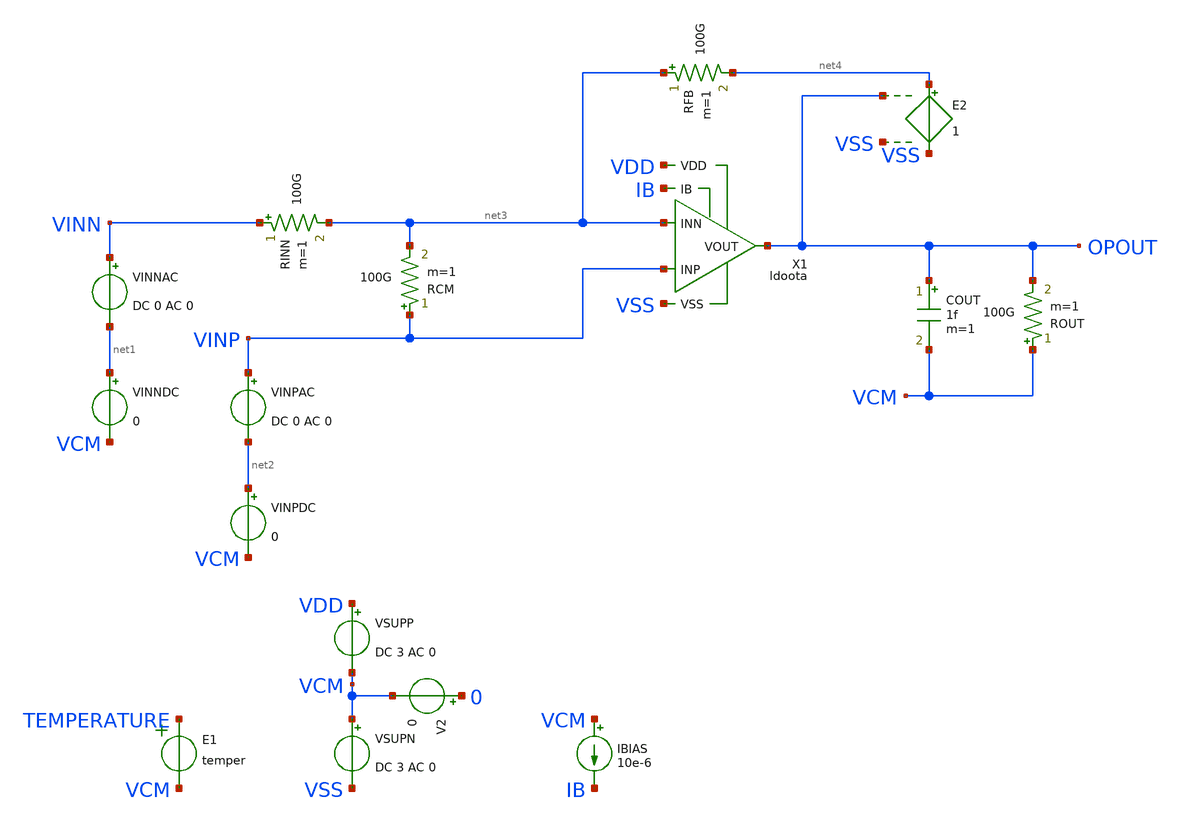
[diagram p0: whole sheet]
** sch_path: tt08/ip/ldo/xschem/ldoota_tb.sch
**.subckt ldoota_tb
V2 0 VCM 0
E1 TEMPERATURE VCM VOL=' temper '
IBIAS VCM IB 10e-6
COUT OPOUT VCM 1f m=1
VINNDC net1 VCM 0
VINNAC VINN net1 DC 0 AC 0
VINPDC net2 VCM 0
VINPAC VINP net2 DC 0 AC 0
ROUT VCM OPOUT 100G m=1
VSUPP VDD VCM DC 3 AC 0
RFB net3 net4 100G m=1
RINN VINN net3 100G m=1
RCM VINP net3 100G m=1
VSUPN VCM VSS DC 3 AC 0
X1 VDD VSS OPOUT IB net3 VINP ldoota
E2 net4 VSS OPOUT VSS 1
**** begin user architecture code

.csparam TB_ID=$::TB_ID\
.csparam MC_RUNS=$::MC_RUNS\
.csparam EXIT_NGSPICE=$::EXIT_NGSPICE\
.lib $::SKYWATER_MODELS/sky130.lib.spice $::CORNER\


* this experimental option enables mos model bin
* selection based on W/NF instead of W
.option wnflag=0

.control
* option savecurrents

* dummy block for goto
if (1)
if TB_ID = 0
	goto AC_INOISE
end
if TB_ID = 1
	goto AC_OL
end
if TB_ID = 2
	goto AC_CMRR_PSRR
end
if TB_ID = 3
	goto TRAN_OUTRNG
end
if TB_ID = 4
	goto TRAN_CMINP
end
if TB_ID = 5
	goto TRAN_SLEW
end
if TB_ID = 6
	goto AC_INOISE
end
if TB_ID = 7
	goto TRAN_THD
end

* Helper Functions
******************
define aunif(nom, avar) (nom+avar*sunif(0))
define agauss(nom, avar, sig) (nom + avar / sig * sgauss (0))

****************************************
label AC_OL
save all
****************************************
if MC_RUNS = 0
	let olgain_1hz = vector(MC_RUNS+1)
	let pm = vector(MC_RUNS+1)
	let ugbw = vector(MC_RUNS+1)
	let f1_3db = vector(MC_RUNS+1)
	let f2_3db = vector(MC_RUNS+1)
	let run=0

	.include ldoota_ac_ol_ops.inc

	set nobreak
	set width=300
	print col olgain_1hz, pm, ugbw, f1_3db, f2_3db > ldoota_ac_ol.csv
else
	let olgain_1hz = vector(MC_RUNS)
	let pm = vector(MC_RUNS)
	let ugbw = vector(MC_RUNS)
	let f1_3db = vector(MC_RUNS)
	let f2_3db = vector(MC_RUNS)
	let run=0
	dowhile run < MC_RUNS
		echo MC-RUN: $&run

		.include ldoota_ac_ol_ops.inc

 		reset
		let run = run + 1
	end
	set nobreak
	set width=300
	print olgain_1hz, pm, ugbw, f1_3db, f2_3db > ldoota_ac_ol.csv
end
goto done

****************************************
label AC_CMRR_PSRR
save all
****************************************
if MC_RUNS = 0
	let cmrr_10Hz = vector(MC_RUNS+1)
	let cmrr_10MHz = vector(MC_RUNS+1)
	let psrr_p_10Hz = vector(MC_RUNS+1)
	let psrr_p_10MHz = vector(MC_RUNS+1)
	let psrr_n_10Hz = vector(MC_RUNS+1)
	let psrr_n_10MHz = vector(MC_RUNS+1)
	let run=0

	.include ldoota_ac_cmrr_psrr_ops.inc

	set nobreak
	set width=300
	print col cmrr_10Hz, cmrr_10MHz, psrr_p_10Hz, psrr_p_10MHz, psrr_n_10Hz, psrr_n_10MHz >
+ ldoota_ac_cmrr_psrr.csv
else
	let cmrr_10Hz = vector(MC_RUNS)
	let cmrr_10MHz = vector(MC_RUNS)
	let psrr_p_10Hz = vector(MC_RUNS)
	let psrr_p_10MHz = vector(MC_RUNS)
	let psrr_n_10Hz = vector(MC_RUNS)
	let psrr_n_10MHz = vector(MC_RUNS)
	let run=0
	dowhile run < MC_RUNS
		echo MC-RUN: $&run

		.include ldoota_ac_cmrr_psrr_ops.inc

 		reset
		let run = run + 1
	end
	set nobreak
	set width=300
	print cmrr_10Hz, cmrr_10MHz, psrr_p_10Hz, psrr_p_10MHz, psrr_n_10Hz, psrr_n_10MHz >
+ ldoota_ac_cmrr_psrr.csv
end
goto done

****************************************
label TRAN_OUTRNG
save all
****************************************
if MC_RUNS = 0
	let neg_out_comp = vector(MC_RUNS+1)
	let pos_out_comp = vector(MC_RUNS+1)
	let run=0

	.include ldoota_tran_outrng_ops.inc

	set nobreak
	set width=300
	print col neg_out_comp, pos_out_comp > ldoota_tran_outrng.csv
else
	let neg_out_comp = vector(MC_RUNS)
	let pos_out_comp = vector(MC_RUNS)
	let run=0
	dowhile run < MC_RUNS
		echo MC-RUN: $&run

		.include ldoota_tran_outrng_ops.inc

 		reset
		let run = run + 1
	end
	set nobreak
	set width=300
	print neg_out_comp, pos_out_comp > ldoota_tran_outrng.csv
end
goto done

****************************************
label TRAN_CMINP
save all
****************************************
if MC_RUNS = 0
	let pos_cm_bound = vector(MC_RUNS+1)
	let neg_cm_bound = vector(MC_RUNS+1)
	let run=0

	.include ldoota_tran_cminp_ops.inc

	set nobreak
	set width=300
	print col pos_cm_bound, neg_cm_bound > ldoota_tran_inprng.csv
else
	let pos_cm_bound = vector(MC_RUNS)
	let neg_cm_bound = vector(MC_RUNS)
	let run=0
	dowhile run < MC_RUNS
		echo MC-RUN: $&run

		.include ldoota_tran_cminp_ops.inc

 		reset
		let run = run + 1
	end
	set nobreak
	set width=300
	print pos_cm_bound, neg_cm_bound > ldoota_tran_inprng.csv
end
goto done

****************************************
label TRAN_SLEW
save all
****************************************
if MC_RUNS = 0
	let inp_offset = vector(MC_RUNS+1)
	let slew_pos = vector(MC_RUNS+1)
	let slew_neg = vector(MC_RUNS+1)
	let run=0

	.include ldoota_tran_slew_ops.inc

	set nobreak
	set width=300
	print col inp_offset, slew_pos, slew_neg > ldoota_tran_slew.csv
else
	let inp_offset = vector(MC_RUNS)
	let slew_pos = vector(MC_RUNS)
	let slew_neg = vector(MC_RUNS)
	let run=0
	dowhile run < MC_RUNS
		echo MC-RUN: $&run

		.include ldoota_tran_slew_ops.inc

 		reset
		let run = run + 1
	end
	set nobreak
	set width=300
	print inp_offset, slew_pos, slew_neg > ldoota_tran_slew.csv
end
goto done

****************************************
label AC_INOISE
****************************************
alter vsupp dc = 3
alter vsupp ac = 0
alter vsupn dc = 3
alter vsupn ac = 0
alter vinnac ac = 0
alter vinndc dc = 0
alter vinpac ac = 0
alter vinpdc dc = 0
alter rinn resistance = 100e12
alter rinn ac = 100e12
alter rcm resistance = 100e12
alter rcm ac = 100e12
alter rfb resistance = 0.01
alter rfb ac = 0.01

noise V(OPOUT) VINPAC dec 10 1 100e6 1
print noise2.onoise_total noise2.inoise_total
if EXIT_NGSPICE = 0
	plot noise1.onoise_spectrum
	plot noise1.inoise_spectrum
end
setplot noise1
write ldoota_noise1_opout.raw all

* https://sourceforge.net/p/ngspice/discussion/120973/thread/2aa3e30f/ -- Holger Vogt
* script to read a specific y-value if x given
**********************************************
let f0 = vector(1)
let f1 = vector(1)
let n_f0 = vector(1)
let n_f1 = vector(1)
compose freq_list values 10 10e3
foreach freq_idx 0 1
	let freq = freq_list[$freq_idx]
	* find index where freqency is just above interesting value
	setplot noise1
	let nn = 0
	while frequency[nn] < freq
		let nn = nn + 1
	end
	* define vectors of frequncies and values just above and below
	* selected frequeny
	let fnn = frequency[nn]
	let nn1 = nn - 1
	let fnn1 = frequency[nn1]
	let snn = onoise_spectrum[nn]
	let snn1 = onoise_spectrum[nn1]
	*print vector values
	echo nn = $&nn  fnn = $&fnn  snn = $&snn
	echo nn1 = $&nn1  fnn1 = $&fnn1  snn1 = $&snn1
	*linear interpolation for exact frequency
	let newsnn = snn1 + (snn - snn1)/(fnn - fnn1)*(freq - fnn1)
	echo newfnn = $&freq  newsnn = $&newsnn
	if $freq_idx = 0
		let f0 = freq
		let n_f0 = newsnn
	end
	if $freq_idx = 1
		let f1 = freq
		let n_f1 = newsnn
	end
end
set nobreak
set width=300
set noprintscale
print col f0, n_f0, f1, n_f1 > ldoota_ac_inoise.csv

goto done

****************************************
label TRAN_THD
save all
****************************************
if MC_RUNS = 0
	let thd = vector(MC_RUNS+1)
	let run=0

	.include ldoota_tran_thd_ops.inc

	set nobreak
	set width=300
	print col thd > ldoota_tran_thd.csv
else
	let thd = vector(MC_RUNS)
	let run=0
	dowhile run < MC_RUNS
		echo MC-RUN: $&run

		reset

		.include ldoota_tran_thd_ops.inc

		let run = run + 1
	end
	set nobreak
	set width=300
	print thd > ldoota_tran_thd.csv
end
goto done

****************************************
label done
****************************************
if EXIT_NGSPICE > 0.0
	exit
end
end
.endc


**** end user architecture code
**.ends

* expanding   symbol:  ldoota.sym # of pins=6
** sym_path: ldoota.sym
** sch_path: ldoota.sch
.subckt ldoota VDD VSS VOUT IB INN INP
*.ipin IB
*.iopin VDD
*.iopin VSS
*.iopin INP
*.iopin INN
*.iopin VOUT
XMMIRL net1 net1 VDD VDD sky130_fd_pr__pfet_g5v0d10v5 L=2 W=20 nf=1 ad='int((nf+1)/2) * W/nf * 0.29'
+ as='int((nf+2)/2) * W/nf * 0.29' pd='2*int((nf+1)/2) * (W/nf + 0.29)' ps='2*int((nf+2)/2) * (W/nf + 0.29)'
+ nrd='0.29 / W' nrs='0.29 / W' sa=0 sb=0 sd=0 mult=1 m=1
XMMIRR net2 net2 VDD VDD sky130_fd_pr__pfet_g5v0d10v5 L=2 W=20 nf=1 ad='int((nf+1)/2) * W/nf * 0.29'
+ as='int((nf+2)/2) * W/nf * 0.29' pd='2*int((nf+1)/2) * (W/nf + 0.29)' ps='2*int((nf+2)/2) * (W/nf + 0.29)'
+ nrd='0.29 / W' nrs='0.29 / W' sa=0 sb=0 sd=0 mult=1 m=1
XMDR net2 INN net3 VSS sky130_fd_pr__nfet_g5v0d10v5 L=2 W=20 nf=1 ad='int((nf+1)/2) * W/nf * 0.29' as='int((nf+2)/2) * W/nf * 0.29'
+ pd='2*int((nf+1)/2) * (W/nf + 0.29)' ps='2*int((nf+2)/2) * (W/nf + 0.29)' nrd='0.29 / W' nrs='0.29 / W'
+ sa=0 sb=0 sd=0 mult=5 m=5
XMDL net1 INP net3 VSS sky130_fd_pr__nfet_g5v0d10v5 L=2 W=20 nf=1 ad='int((nf+1)/2) * W/nf * 0.29' as='int((nf+2)/2) * W/nf * 0.29'
+ pd='2*int((nf+1)/2) * (W/nf + 0.29)' ps='2*int((nf+2)/2) * (W/nf + 0.29)' nrd='0.29 / W' nrs='0.29 / W'
+ sa=0 sb=0 sd=0 mult=5 m=5
XMMIR2 net3 IB VSS VSS sky130_fd_pr__nfet_g5v0d10v5 L=2 W=20 nf=1 ad='int((nf+1)/2) * W/nf * 0.29' as='int((nf+2)/2) * W/nf * 0.29'
+ pd='2*int((nf+1)/2) * (W/nf + 0.29)' ps='2*int((nf+2)/2) * (W/nf + 0.29)' nrd='0.29 / W' nrs='0.29 / W'
+ sa=0 sb=0 sd=0 mult=1 m=1
XMO vot net2 VDD VDD sky130_fd_pr__pfet_g5v0d10v5 L=2 W=20 nf=1 ad='int((nf+1)/2) * W/nf * 0.29' as='int((nf+2)/2) * W/nf * 0.29'
+ pd='2*int((nf+1)/2) * (W/nf + 0.29)' ps='2*int((nf+2)/2) * (W/nf + 0.29)' nrd='0.29 / W' nrs='0.29 / W'
+ sa=0 sb=0 sd=0 mult=5 m=5
XMMIRL1 net4 net1 VDD VDD sky130_fd_pr__pfet_g5v0d10v5 L=2 W=20 nf=1 ad='int((nf+1)/2) * W/nf * 0.29'
+ as='int((nf+2)/2) * W/nf * 0.29' pd='2*int((nf+1)/2) * (W/nf + 0.29)' ps='2*int((nf+2)/2) * (W/nf + 0.29)'
+ nrd='0.29 / W' nrs='0.29 / W' sa=0 sb=0 sd=0 mult=1 m=1
XMMIRL2 net4 net4 VSS VSS sky130_fd_pr__nfet_g5v0d10v5 L=2 W=20 nf=1 ad='int((nf+1)/2) * W/nf * 0.29'
+ as='int((nf+2)/2) * W/nf * 0.29' pd='2*int((nf+1)/2) * (W/nf + 0.29)' ps='2*int((nf+2)/2) * (W/nf + 0.29)'
+ nrd='0.29 / W' nrs='0.29 / W' sa=0 sb=0 sd=0 mult=1 m=1
XMMIR3 vot net4 VSS VSS sky130_fd_pr__nfet_g5v0d10v5 L=2 W=20 nf=1 ad='int((nf+1)/2) * W/nf * 0.29' as='int((nf+2)/2) * W/nf * 0.29'
+ pd='2*int((nf+1)/2) * (W/nf + 0.29)' ps='2*int((nf+2)/2) * (W/nf + 0.29)' nrd='0.29 / W' nrs='0.29 / W'
+ sa=0 sb=0 sd=0 mult=5 m=5
XMOT VOUT vot VDD VDD sky130_fd_pr__pfet_g5v0d10v5 L=0.5 W=20 nf=1 ad='int((nf+1)/2) * W/nf * 0.29' as='int((nf+2)/2) * W/nf * 0.29'
+ pd='2*int((nf+1)/2) * (W/nf + 0.29)' ps='2*int((nf+2)/2) * (W/nf + 0.29)' nrd='0.29 / W' nrs='0.29 / W'
+ sa=0 sb=0 sd=0 mult=20 m=20
XMOB VOUT IB VSS VSS sky130_fd_pr__nfet_g5v0d10v5 L=2 W=20 nf=1 ad='int((nf+1)/2) * W/nf * 0.29' as='int((nf+2)/2) * W/nf * 0.29'
+ pd='2*int((nf+1)/2) * (W/nf + 0.29)' ps='2*int((nf+2)/2) * (W/nf + 0.29)' nrd='0.29 / W' nrs='0.29 / W'
+ sa=0 sb=0 sd=0 mult=4 m=4
XC1 net5 vot sky130_fd_pr__cap_mim_m3_1 W=20 L=20 MF=16 m=16
XMMIR1 IB IB VSS VSS sky130_fd_pr__nfet_g5v0d10v5 L=2 W=20 nf=1 ad='int((nf+1)/2) * W/nf * 0.29' as='int((nf+2)/2) * W/nf * 0.29'
+ pd='2*int((nf+1)/2) * (W/nf + 0.29)' ps='2*int((nf+2)/2) * (W/nf + 0.29)' nrd='0.29 / W' nrs='0.29 / W'
+ sa=0 sb=0 sd=0 mult=1 m=1
XR1 net5 VOUT VSS sky130_fd_pr__res_xhigh_po_1p41 L=2 mult=1 m=1
XMMIRL3 VDD VDD VDD VDD sky130_fd_pr__pfet_g5v0d10v5 L=2 W=10 nf=1 ad='int((nf+1)/2) * W/nf * 0.29' as='int((nf+2)/2) * W/nf * 0.29'
+ pd='2*int((nf+1)/2) * (W/nf + 0.29)' ps='2*int((nf+2)/2) * (W/nf + 0.29)' nrd='0.29 / W' nrs='0.29 / W'
+ sa=0 sb=0 sd=0 mult=1 m=1
XMMIRL4 VDD VDD VDD VDD sky130_fd_pr__pfet_g5v0d10v5 L=2 W=10 nf=1 ad='int((nf+1)/2) * W/nf * 0.29' as='int((nf+2)/2) * W/nf * 0.29'
+ pd='2*int((nf+1)/2) * (W/nf + 0.29)' ps='2*int((nf+2)/2) * (W/nf + 0.29)' nrd='0.29 / W' nrs='0.29 / W'
+ sa=0 sb=0 sd=0 mult=1 m=1
XMMIRR1 VDD VDD VDD VDD sky130_fd_pr__pfet_g5v0d10v5 L=2 W=10 nf=1 ad='int((nf+1)/2) * W/nf * 0.29' as='int((nf+2)/2) * W/nf * 0.29'
+ pd='2*int((nf+1)/2) * (W/nf + 0.29)' ps='2*int((nf+2)/2) * (W/nf + 0.29)' nrd='0.29 / W' nrs='0.29 / W'
+ sa=0 sb=0 sd=0 mult=1 m=1
XMO1 VDD VDD VDD VDD sky130_fd_pr__pfet_g5v0d10v5 L=2 W=10 nf=1 ad='int((nf+1)/2) * W/nf * 0.29' as='int((nf+2)/2) * W/nf * 0.29'
+ pd='2*int((nf+1)/2) * (W/nf + 0.29)' ps='2*int((nf+2)/2) * (W/nf + 0.29)' nrd='0.29 / W' nrs='0.29 / W'
+ sa=0 sb=0 sd=0 mult=1 m=1
XMMIR4 VSS VSS VSS VSS sky130_fd_pr__nfet_g5v0d10v5 L=2 W=10 nf=1 ad='int((nf+1)/2) * W/nf * 0.29' as='int((nf+2)/2) * W/nf * 0.29'
+ pd='2*int((nf+1)/2) * (W/nf + 0.29)' ps='2*int((nf+2)/2) * (W/nf + 0.29)' nrd='0.29 / W' nrs='0.29 / W'
+ sa=0 sb=0 sd=0 mult=1 m=1
XMMIRL5 VSS VSS VSS VSS sky130_fd_pr__nfet_g5v0d10v5 L=2 W=10 nf=1 ad='int((nf+1)/2) * W/nf * 0.29' as='int((nf+2)/2) * W/nf * 0.29'
+ pd='2*int((nf+1)/2) * (W/nf + 0.29)' ps='2*int((nf+2)/2) * (W/nf + 0.29)' nrd='0.29 / W' nrs='0.29 / W'
+ sa=0 sb=0 sd=0 mult=1 m=1
XMDL1 VSS VSS VSS VSS sky130_fd_pr__nfet_g5v0d10v5 L=2 W=20 nf=1 ad='int((nf+1)/2) * W/nf * 0.29' as='int((nf+2)/2) * W/nf * 0.29'
+ pd='2*int((nf+1)/2) * (W/nf + 0.29)' ps='2*int((nf+2)/2) * (W/nf + 0.29)' nrd='0.29 / W' nrs='0.29 / W'
+ sa=0 sb=0 sd=0 mult=1 m=1
XMDR1 VSS VSS VSS VSS sky130_fd_pr__nfet_g5v0d10v5 L=2 W=20 nf=1 ad='int((nf+1)/2) * W/nf * 0.29' as='int((nf+2)/2) * W/nf * 0.29'
+ pd='2*int((nf+1)/2) * (W/nf + 0.29)' ps='2*int((nf+2)/2) * (W/nf + 0.29)' nrd='0.29 / W' nrs='0.29 / W'
+ sa=0 sb=0 sd=0 mult=1 m=1
XMMIR5 VSS VSS VSS VSS sky130_fd_pr__nfet_g5v0d10v5 L=2 W=10 nf=1 ad='int((nf+1)/2) * W/nf * 0.29' as='int((nf+2)/2) * W/nf * 0.29'
+ pd='2*int((nf+1)/2) * (W/nf + 0.29)' ps='2*int((nf+2)/2) * (W/nf + 0.29)' nrd='0.29 / W' nrs='0.29 / W'
+ sa=0 sb=0 sd=0 mult=1 m=1
XMOB1 VSS VSS VSS VSS sky130_fd_pr__nfet_g5v0d10v5 L=2 W=10 nf=1 ad='int((nf+1)/2) * W/nf * 0.29' as='int((nf+2)/2) * W/nf * 0.29'
+ pd='2*int((nf+1)/2) * (W/nf + 0.29)' ps='2*int((nf+2)/2) * (W/nf + 0.29)' nrd='0.29 / W' nrs='0.29 / W'
+ sa=0 sb=0 sd=0 mult=1 m=1
.ends

.end
